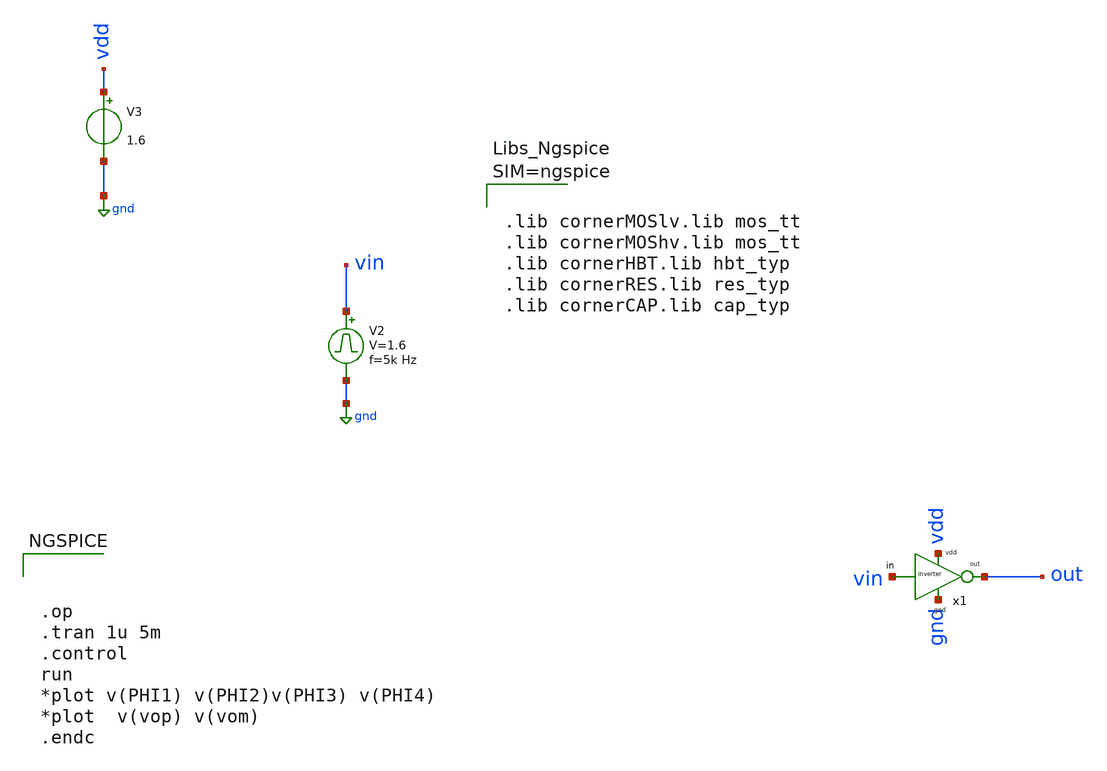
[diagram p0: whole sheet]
** sch_path: Clock_gen_using_transistor_hv/temp.sch
**.subckt temp
V2 vin gnd pulse 0 1.6 '0.495/ 5k ' '0.01/5k ' '0.01/5k ' '0.49/5k ' '1/5k '
V3 vdd gnd 1.6
x1 vin out vdd gnd inverter
**** begin user architecture code



.lib cornerMOSlv.lib mos_tt
.lib cornerMOShv.lib mos_tt
.lib cornerHBT.lib hbt_typ
.lib cornerRES.lib res_typ
.lib cornerCAP.lib cap_typ






.op
.tran 1u 5m
.control
run
*plot v(PHI1) v(PHI2)v(PHI3) v(PHI4)
*plot  v(vop) v(vom)
.endc


**** end user architecture code
**.ends

* expanding   symbol:
*+  /home/designer/shared/uni_cass/final_Design_file/Clock_gen_using_transistor_hv/inverter.sym # of pins=4
** sym_path: /home/designer/shared/uni_cass/final_Design_file/Clock_gen_using_transistor_hv/inverter.sym
** sch_path: /home/designer/shared/uni_cass/final_Design_file/Clock_gen_using_transistor_hv/inverter.sch
.subckt inverter in out vdd gnd
*.iopin in
*.iopin vdd
*.iopin out
*.iopin gnd
XM3 out in vdd vdd sg13_hv_pmos w=2u l=2u ng=1 m=1 mm_ok=1
XM1 out in gnd gnd sg13_hv_nmos w=1u l=1u ng=1 m=1 mm_ok=1
.ends

.GLOBAL gnd
.end
